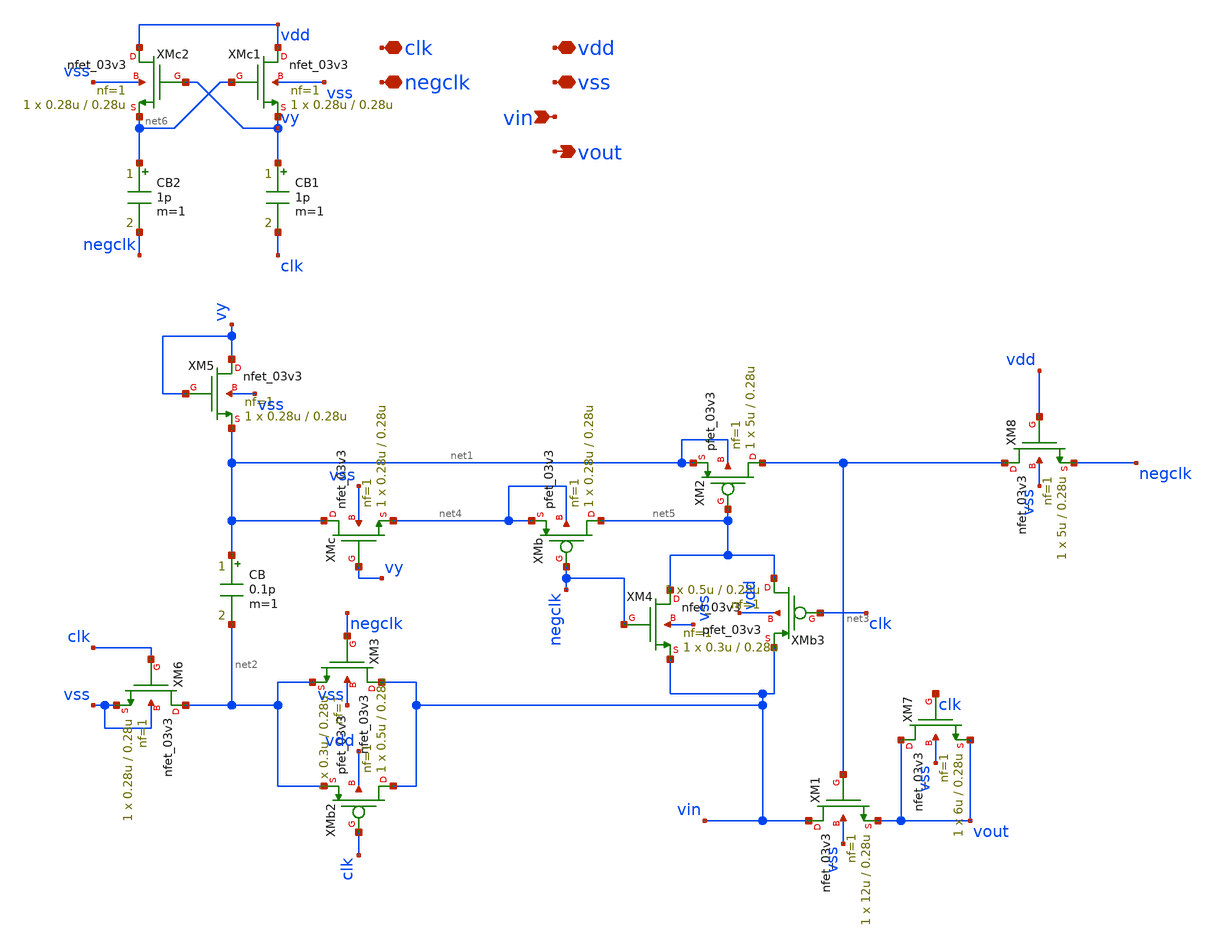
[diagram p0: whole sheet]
** sch_path: xschem/designs/bootstrap_sw.sch
**.subckt bootstrap_sw vdd vss vin vout clk negclk
*.iopin vdd
*.iopin vss
*.ipin vin
*.opin vout
*.iopin clk
*.iopin negclk
XM1 vin net3 vout vss nfet_03v3 L=0.28u W=12u nf=1 ad='int((nf+1)/2) * W/nf * 0.18u' as='int((nf+2)/2) * W/nf * 0.18u'
+ pd='2*int((nf+1)/2) * (W/nf + 0.18u)' ps='2*int((nf+2)/2) * (W/nf + 0.18u)' nrd='0.18u / W' nrs='0.18u / W'
+ sa=0 sb=0 sd=0 m=1
XM2 net3 net5 net1 net1 pfet_03v3 L=0.28u W=5u nf=1 ad='int((nf+1)/2) * W/nf * 0.18u' as='int((nf+2)/2) * W/nf * 0.18u'
+ pd='2*int((nf+1)/2) * (W/nf + 0.18u)' ps='2*int((nf+2)/2) * (W/nf + 0.18u)' nrd='0.18u / W' nrs='0.18u / W'
+ sa=0 sb=0 sd=0 m=1
XM3 vin negclk net2 vss nfet_03v3 L=0.28u W=0.3u nf=1 ad='int((nf+1)/2) * W/nf * 0.18u' as='int((nf+2)/2) * W/nf * 0.18u'
+ pd='2*int((nf+1)/2) * (W/nf + 0.18u)' ps='2*int((nf+2)/2) * (W/nf + 0.18u)' nrd='0.18u / W' nrs='0.18u / W'
+ sa=0 sb=0 sd=0 m=1
XM8 net3 vdd negclk vss nfet_03v3 L=0.28u W=5u nf=1 ad='int((nf+1)/2) * W/nf * 0.18u' as='int((nf+2)/2) * W/nf * 0.18u'
+ pd='2*int((nf+1)/2) * (W/nf + 0.18u)' ps='2*int((nf+2)/2) * (W/nf + 0.18u)' nrd='0.18u / W' nrs='0.18u / W'
+ sa=0 sb=0 sd=0 m=1
XM6 net2 clk vss vss nfet_03v3 L=0.28u W=0.28u nf=1 ad='int((nf+1)/2) * W/nf * 0.18u' as='int((nf+2)/2) * W/nf * 0.18u'
+ pd='2*int((nf+1)/2) * (W/nf + 0.18u)' ps='2*int((nf+2)/2) * (W/nf + 0.18u)' nrd='0.18u / W' nrs='0.18u / W'
+ sa=0 sb=0 sd=0 m=1
CB net1 net2 0.1p m=1
XMb net5 negclk net4 net4 pfet_03v3 L=0.28u W=0.28u nf=1 ad='int((nf+1)/2) * W/nf * 0.18u' as='int((nf+2)/2) * W/nf * 0.18u'
+ pd='2*int((nf+1)/2) * (W/nf + 0.18u)' ps='2*int((nf+2)/2) * (W/nf + 0.18u)' nrd='0.18u / W' nrs='0.18u / W'
+ sa=0 sb=0 sd=0 m=1
XMc net1 vy net4 vss nfet_03v3 L=0.28u W=0.28u nf=1 ad='int((nf+1)/2) * W/nf * 0.18u' as='int((nf+2)/2) * W/nf * 0.18u'
+ pd='2*int((nf+1)/2) * (W/nf + 0.18u)' ps='2*int((nf+2)/2) * (W/nf + 0.18u)' nrd='0.18u / W' nrs='0.18u / W'
+ sa=0 sb=0 sd=0 m=1
XMb2 vin clk net2 vdd pfet_03v3 L=0.28u W=0.5u nf=1 ad='int((nf+1)/2) * W/nf * 0.18u' as='int((nf+2)/2) * W/nf * 0.18u'
+ pd='2*int((nf+1)/2) * (W/nf + 0.18u)' ps='2*int((nf+2)/2) * (W/nf + 0.18u)' nrd='0.18u / W' nrs='0.18u / W'
+ sa=0 sb=0 sd=0 m=1
XM4 net5 negclk vin vss nfet_03v3 L=0.28u W=0.3u nf=1 ad='int((nf+1)/2) * W/nf * 0.18u' as='int((nf+2)/2) * W/nf * 0.18u'
+ pd='2*int((nf+1)/2) * (W/nf + 0.18u)' ps='2*int((nf+2)/2) * (W/nf + 0.18u)' nrd='0.18u / W' nrs='0.18u / W'
+ sa=0 sb=0 sd=0 m=1
XMb3 net5 clk vin vdd pfet_03v3 L=0.28u W=0.5u nf=1 ad='int((nf+1)/2) * W/nf * 0.18u' as='int((nf+2)/2) * W/nf * 0.18u'
+ pd='2*int((nf+1)/2) * (W/nf + 0.18u)' ps='2*int((nf+2)/2) * (W/nf + 0.18u)' nrd='0.18u / W' nrs='0.18u / W'
+ sa=0 sb=0 sd=0 m=1
XM5 vy vy net1 vss nfet_03v3 L=0.28u W=0.28u nf=1 ad='int((nf+1)/2) * W/nf * 0.18u' as='int((nf+2)/2) * W/nf * 0.18u'
+ pd='2*int((nf+1)/2) * (W/nf + 0.18u)' ps='2*int((nf+2)/2) * (W/nf + 0.18u)' nrd='0.18u / W' nrs='0.18u / W'
+ sa=0 sb=0 sd=0 m=1
XMc1 vdd net6 vy vss nfet_03v3 L=0.28u W=0.28u nf=1 ad='int((nf+1)/2) * W/nf * 0.18u' as='int((nf+2)/2) * W/nf * 0.18u'
+ pd='2*int((nf+1)/2) * (W/nf + 0.18u)' ps='2*int((nf+2)/2) * (W/nf + 0.18u)' nrd='0.18u / W' nrs='0.18u / W'
+ sa=0 sb=0 sd=0 m=1
XMc2 vdd vy net6 vss nfet_03v3 L=0.28u W=0.28u nf=1 ad='int((nf+1)/2) * W/nf * 0.18u' as='int((nf+2)/2) * W/nf * 0.18u'
+ pd='2*int((nf+1)/2) * (W/nf + 0.18u)' ps='2*int((nf+2)/2) * (W/nf + 0.18u)' nrd='0.18u / W' nrs='0.18u / W'
+ sa=0 sb=0 sd=0 m=1
CB1 vy clk 1p m=1
CB2 net6 negclk 1p m=1
XM7 vout clk vout vss nfet_03v3 L=0.28u W=6u nf=1 ad='int((nf+1)/2) * W/nf * 0.18u' as='int((nf+2)/2) * W/nf * 0.18u'
+ pd='2*int((nf+1)/2) * (W/nf + 0.18u)' ps='2*int((nf+2)/2) * (W/nf + 0.18u)' nrd='0.18u / W' nrs='0.18u / W'
+ sa=0 sb=0 sd=0 m=1
**.ends
.end
